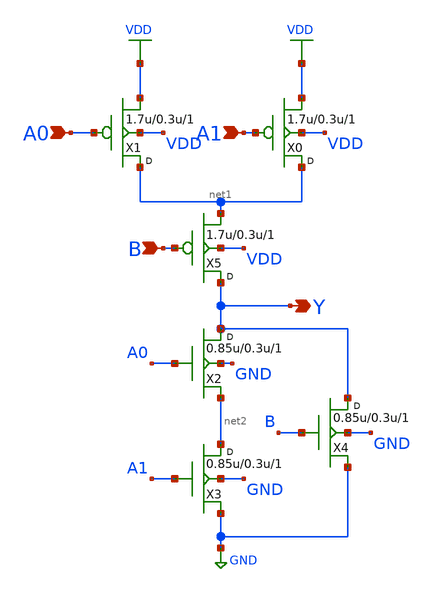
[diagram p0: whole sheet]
** sch_path: lib/xschem/gf180mcu_osu_sc_12T_aoi21_1.sch
**.subckt gf180mcu_osu_sc_12T_aoi21_1 A0 A1 Y B
*.ipin A0
*.ipin A1
*.opin Y
*.ipin B
X1 net1 A0 VDD VDD pmos_3p3 w=1.7u l=0.3u m=1
X0 net1 A1 VDD VDD pmos_3p3 w=1.7u l=0.3u m=1
X2 Y A0 net2 GND nmos_3p3 w=0.85u l=0.3u m=1
X3 net2 A1 GND GND nmos_3p3 w=0.85u l=0.3u m=1
X4 Y B GND GND nmos_3p3 w=0.85u l=0.3u m=1
X5 Y B net1 VDD pmos_3p3 w=1.7u l=0.3u m=1
**** begin user architecture code


.inc "/import/yukari1/lrburle/OSU_180/char/techfiles/design.hspice"
.lib "/import/yukari1/lrburle/OSU_180/char/techfiles/sm141064.hspice" typical


**** end user architecture code
**.ends
.GLOBAL VDD
.GLOBAL GND
.end
